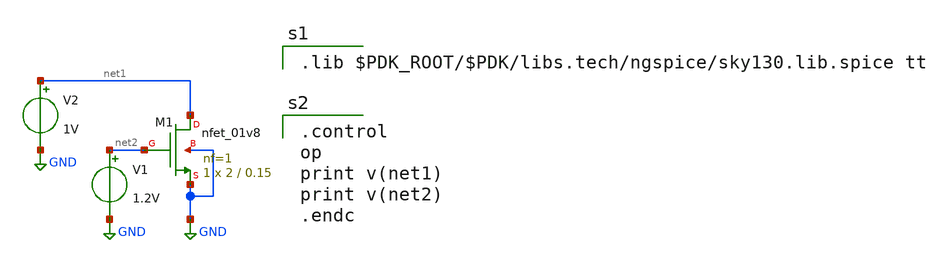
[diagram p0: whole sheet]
** sch_path: schematics/sky130_nmos_test.sch
**.subckt sky130_nmos_test
XM1 net1 net2 GND GND sky130_fd_pr__nfet_01v8 L=0.15 W=2 nf=1 ad='int((nf+1)/2) * W/nf * 0.29' as='int((nf+2)/2) * W/nf * 0.29'
+ pd='2*int((nf+1)/2) * (W/nf + 0.29)' ps='2*int((nf+2)/2) * (W/nf + 0.29)' nrd='0.29 / W' nrs='0.29 / W'
+ sa=0 sb=0 sd=0 mult=1 m=1
V1 net2 GND 1.2V
V2 net1 GND 1V
**** begin user architecture code

.lib $PDK_ROOT/$PDK/libs.tech/ngspice/sky130.lib.spice tt


.control
op
print v(net1)
print v(net2)
.endc

**** end user architecture code
**.ends
.GLOBAL GND
.end
